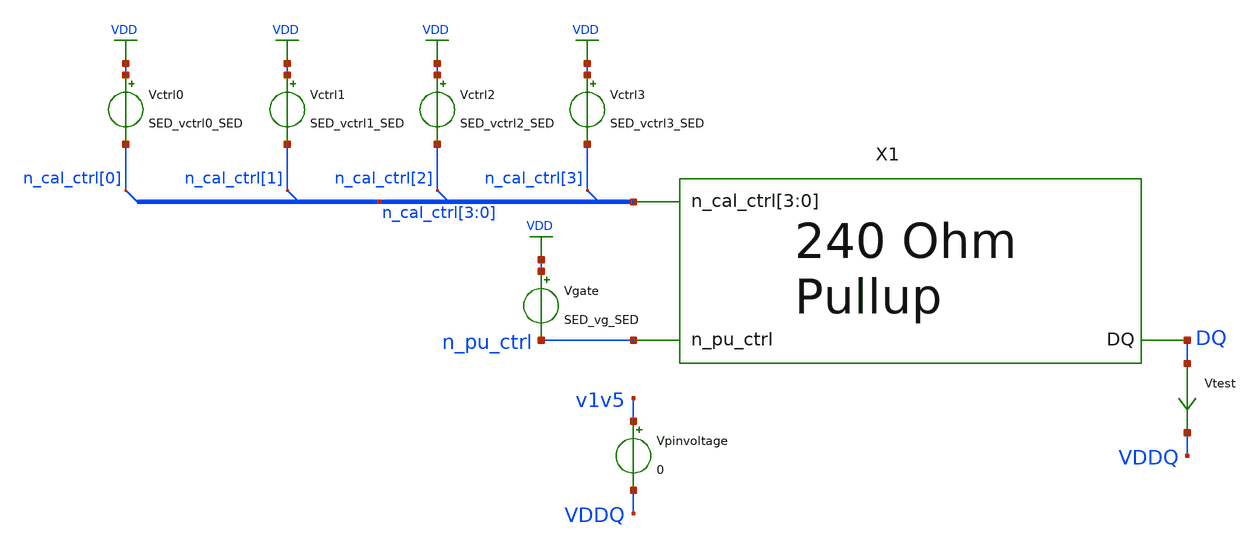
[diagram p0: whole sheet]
** sch_path: schem/p-leg_tb.sch
* Copyright 2021 Stefan Frederik Schippers
* Licensed under the Apache License, Version 2.0 (the "License");
* you may not use this file except in compliance with the License.
* You may obtain a copy of the License at
* https://www.apache.org/licenses/LICENSE-2.0
* Unless required by applicable law or agreed to in writing, software
* distributed under the License is distributed on an "AS IS" BASIS,
* WITHOUT WARRANTIES OR CONDITIONS OF ANY KIND, either express or implied.
* See the License for the specific language governing permissions and
* limitations under the License.
**.subckt p-leg_tb
Vctrl0 VDD n_cal_ctrl[0] SED_vctrl0_SED
Vctrl1 VDD n_cal_ctrl[1] SED_vctrl1_SED
Vctrl2 VDD n_cal_ctrl[2] SED_vctrl2_SED
Vctrl3 VDD n_cal_ctrl[3] SED_vctrl3_SED
Vgate VDD n_pu_ctrl SED_vg_SED
Vtest DQ VDDQ 0
.save i(vtest)
Vpinvoltage v1v5 VDDQ 0
X1 DQ n_pu_ctrl n_cal_ctrl[3] n_cal_ctrl[2] n_cal_ctrl[1] n_cal_ctrl[0] p-leg
**** begin user architecture code
 ** Local library links to pdk
.lib ./sky130/libs/SED_process_SED_lib.spice SED_process_SED

**** end user architecture code
**.ends

* expanding   symbol:  p-leg.sym # of pins=3
** sym_path: schem/p-leg.sym
** sch_path: schem/p-leg.sch
.subckt p-leg DQ n_pu_ctrl n_cal_ctrl[3] n_cal_ctrl[2] n_cal_ctrl[1] n_cal_ctrl[0]
*.ipin n_cal_ctrl[3],n_cal_ctrl[2],n_cal_ctrl[1],n_cal_ctrl[0]
*.ipin n_pu_ctrl
*.iopin DQ
XR1 DQ net1 sky130_fd_pr__res_generic_po W=0.33 L=1.8 m=1
XMpullup net1 n_pu_ctrl VDD VDD sky130_fd_pr__pfet_01v8_lvt L=0.35 W=1 nf=1 ad='int((nf+1)/2) * W/nf * 0.29'
+ as='int((nf+2)/2) * W/nf * 0.29' pd='2*int((nf+1)/2) * (W/nf + 0.29)' ps='2*int((nf+2)/2) * (W/nf + 0.29)'
+ nrd='0.29 / W' nrs='0.29 / W' sa=0 sb=0 sd=0 mult=128 m=128
XMctrltot VDD n_cal_ctrl[0] VDD VDD sky130_fd_pr__pfet_01v8_lvt L=0.35 W=1 nf=1 ad='int((nf+1)/2) * W/nf * 0.29'
+ as='int((nf+2)/2) * W/nf * 0.29' pd='2*int((nf+1)/2) * (W/nf + 0.29)' ps='2*int((nf+2)/2) * (W/nf + 0.29)'
+ nrd='0.29 / W' nrs='0.29 / W' sa=0 sb=0 sd=0 mult=120 m=120
XMctrl0 DQ n_cal_ctrl[0] net1 VDD sky130_fd_pr__pfet_01v8_lvt L=0.35 W=1 nf=1 ad='int((nf+1)/2) * W/nf * 0.29'
+ as='int((nf+2)/2) * W/nf * 0.29' pd='2*int((nf+1)/2) * (W/nf + 0.29)' ps='2*int((nf+2)/2) * (W/nf + 0.29)'
+ nrd='0.29 / W' nrs='0.29 / W' sa=0 sb=0 sd=0 mult=48 m=48
XMctrl1 DQ n_cal_ctrl[1] net1 VDD sky130_fd_pr__pfet_01v8_lvt L=0.35 W=1 nf=1 ad='int((nf+1)/2) * W/nf * 0.29'
+ as='int((nf+2)/2) * W/nf * 0.29' pd='2*int((nf+1)/2) * (W/nf + 0.29)' ps='2*int((nf+2)/2) * (W/nf + 0.29)'
+ nrd='0.29 / W' nrs='0.29 / W' sa=0 sb=0 sd=0 mult=16 m=16
XMctrl2 DQ n_cal_ctrl[2] net1 VDD sky130_fd_pr__pfet_01v8_lvt L=0.35 W=1 nf=1 ad='int((nf+1)/2) * W/nf * 0.29'
+ as='int((nf+2)/2) * W/nf * 0.29' pd='2*int((nf+1)/2) * (W/nf + 0.29)' ps='2*int((nf+2)/2) * (W/nf + 0.29)'
+ nrd='0.29 / W' nrs='0.29 / W' sa=0 sb=0 sd=0 mult=8 m=8
XMctrl3 DQ n_cal_ctrl[3] net1 VDD sky130_fd_pr__pfet_01v8_lvt L=0.35 W=1 nf=1 ad='int((nf+1)/2) * W/nf * 0.29'
+ as='int((nf+2)/2) * W/nf * 0.29' pd='2*int((nf+1)/2) * (W/nf + 0.29)' ps='2*int((nf+2)/2) * (W/nf + 0.29)'
+ nrd='0.29 / W' nrs='0.29 / W' sa=0 sb=0 sd=0 mult=4 m=4
.ends

.GLOBAL VDD
**** begin user architecture code



* power voltage
vvdd VDD 0 SED_vdd_SED
vv1v5 v1v5 0 1.5

.control
save all
set temp=SED_temp_SED

* RUN SIMULATION
dc Vpinvoltage 0.3 1.2 0.05
* OUTPUT
print (SED_vdd_SED-vddq)/i(vtest)
wrdata out/SED_plotName_SED/SED_plotName_SED.txt (SED_vdd_SED-vddq)/i(vtest)
set hcopydevtype = svg
hardcopy ./out/SED_plotName_SED/SED_plotName_SED.svg (SED_vdd_SED-vddq)/I(vtest) vs vddq title 'Resistance vs pin voltage'

.endc


**** end user architecture code
.end
